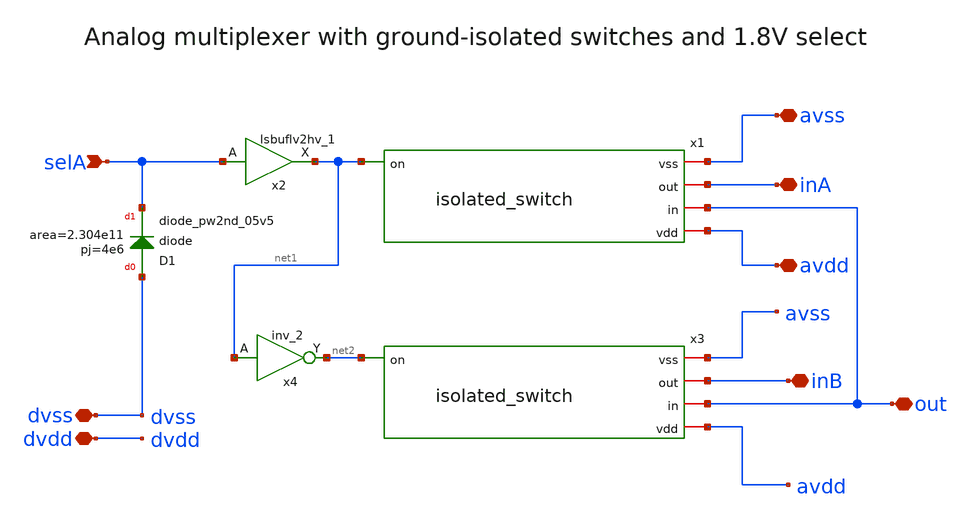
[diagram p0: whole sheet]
** sch_path: xschem/analog_mux_sel1v8.sch
**.subckt analog_mux_sel1v8 selA avss out inA avdd inB dvdd dvss
*.ipin selA
*.iopin avss
*.iopin out
*.iopin inA
*.iopin avdd
*.iopin inB
*.iopin dvdd
*.iopin dvss
x1 net1 avss inA out avdd isolated_switch
x2 selA dvdd dvss dvss avdd avdd net1 sky130_fd_sc_hvl__lsbuflv2hv_1
x3 net2 avss inB out avdd isolated_switch
x4 net1 dvss dvss avdd avdd net2 sky130_fd_sc_hvl__inv_2
XD1 dvss selA sky130_fd_pr__diode_pw2nd_05v5 area=2.304e11 pj=4e6
**.ends

* expanding   symbol:  isolated_switch.sym # of pins=5
** sym_path: xschem/isolated_switch.sym
** sch_path: xschem/isolated_switch.sch
.subckt isolated_switch on vss out in vdd
*.ipin on
*.iopin out
*.iopin vdd
*.iopin vss
*.iopin in
XM1 in onp net1 vss sky130_fd_pr__nfet_g5v0d10v5 L=0.5 W=8 nf=2 ad='int((nf+1)/2) * W/nf * 0.29' as='int((nf+2)/2) * W/nf * 0.29'
+ pd='2*int((nf+1)/2) * (W/nf + 0.29)' ps='2*int((nf+2)/2) * (W/nf + 0.29)' nrd='0.29 / W' nrs='0.29 / W'
+ sa=0 sb=0 sd=0 mult=1 m=1
XM2 in onb net1 vdd sky130_fd_pr__pfet_g5v0d10v5 L=0.5 W=4 nf=2 ad='int((nf+1)/2) * W/nf * 0.29' as='int((nf+2)/2) * W/nf * 0.29'
+ pd='2*int((nf+1)/2) * (W/nf + 0.29)' ps='2*int((nf+2)/2) * (W/nf + 0.29)' nrd='0.29 / W' nrs='0.29 / W'
+ sa=0 sb=0 sd=0 mult=1 m=1
XM3 net1 onb net1 vss sky130_fd_pr__nfet_g5v0d10v5 L=0.5 W=4 nf=1 ad='int((nf+1)/2) * W/nf * 0.29' as='int((nf+2)/2) * W/nf * 0.29'
+ pd='2*int((nf+1)/2) * (W/nf + 0.29)' ps='2*int((nf+2)/2) * (W/nf + 0.29)' nrd='0.29 / W' nrs='0.29 / W'
+ sa=0 sb=0 sd=0 mult=1 m=1
XM4 net1 onp net1 vdd sky130_fd_pr__pfet_g5v0d10v5 L=0.5 W=2 nf=1 ad='int((nf+1)/2) * W/nf * 0.29' as='int((nf+2)/2) * W/nf * 0.29'
+ pd='2*int((nf+1)/2) * (W/nf + 0.29)' ps='2*int((nf+2)/2) * (W/nf + 0.29)' nrd='0.29 / W' nrs='0.29 / W'
+ sa=0 sb=0 sd=0 mult=1 m=1
XM5 in onb in vss sky130_fd_pr__nfet_g5v0d10v5 L=0.5 W=4 nf=1 ad='int((nf+1)/2) * W/nf * 0.29' as='int((nf+2)/2) * W/nf * 0.29'
+ pd='2*int((nf+1)/2) * (W/nf + 0.29)' ps='2*int((nf+2)/2) * (W/nf + 0.29)' nrd='0.29 / W' nrs='0.29 / W'
+ sa=0 sb=0 sd=0 mult=1 m=1
XM6 in onp in vdd sky130_fd_pr__pfet_g5v0d10v5 L=0.5 W=2 nf=1 ad='int((nf+1)/2) * W/nf * 0.29' as='int((nf+2)/2) * W/nf * 0.29'
+ pd='2*int((nf+1)/2) * (W/nf + 0.29)' ps='2*int((nf+2)/2) * (W/nf + 0.29)' nrd='0.29 / W' nrs='0.29 / W'
+ sa=0 sb=0 sd=0 mult=1 m=1
XM7 onb on vdd vdd sky130_fd_pr__pfet_g5v0d10v5 L=0.5 W=2 nf=2 ad='int((nf+1)/2) * W/nf * 0.29' as='int((nf+2)/2) * W/nf * 0.29'
+ pd='2*int((nf+1)/2) * (W/nf + 0.29)' ps='2*int((nf+2)/2) * (W/nf + 0.29)' nrd='0.29 / W' nrs='0.29 / W'
+ sa=0 sb=0 sd=0 mult=1 m=1
XM8 onb on vss vss sky130_fd_pr__nfet_g5v0d10v5 L=0.5 W=2 nf=1 ad='int((nf+1)/2) * W/nf * 0.29' as='int((nf+2)/2) * W/nf * 0.29'
+ pd='2*int((nf+1)/2) * (W/nf + 0.29)' ps='2*int((nf+2)/2) * (W/nf + 0.29)' nrd='0.29 / W' nrs='0.29 / W'
+ sa=0 sb=0 sd=0 mult=1 m=1
XM9 onp onb vdd vdd sky130_fd_pr__pfet_g5v0d10v5 L=0.5 W=2 nf=2 ad='int((nf+1)/2) * W/nf * 0.29' as='int((nf+2)/2) * W/nf * 0.29'
+ pd='2*int((nf+1)/2) * (W/nf + 0.29)' ps='2*int((nf+2)/2) * (W/nf + 0.29)' nrd='0.29 / W' nrs='0.29 / W'
+ sa=0 sb=0 sd=0 mult=1 m=1
XM10 onp onb vss vss sky130_fd_pr__nfet_g5v0d10v5 L=0.5 W=2 nf=1 ad='int((nf+1)/2) * W/nf * 0.29' as='int((nf+2)/2) * W/nf * 0.29'
+ pd='2*int((nf+1)/2) * (W/nf + 0.29)' ps='2*int((nf+2)/2) * (W/nf + 0.29)' nrd='0.29 / W' nrs='0.29 / W'
+ sa=0 sb=0 sd=0 mult=1 m=1
XXD1 vss on sky130_fd_pr__diode_pw2nd_05v5 area=2.025e11 pj=4e6
XM11 net1 onp out vss sky130_fd_pr__nfet_g5v0d10v5 L=0.5 W=8 nf=2 ad='int((nf+1)/2) * W/nf * 0.29' as='int((nf+2)/2) * W/nf * 0.29'
+ pd='2*int((nf+1)/2) * (W/nf + 0.29)' ps='2*int((nf+2)/2) * (W/nf + 0.29)' nrd='0.29 / W' nrs='0.29 / W'
+ sa=0 sb=0 sd=0 mult=1 m=1
XM12 net1 onb out vdd sky130_fd_pr__pfet_g5v0d10v5 L=0.5 W=4 nf=2 ad='int((nf+1)/2) * W/nf * 0.29' as='int((nf+2)/2) * W/nf * 0.29'
+ pd='2*int((nf+1)/2) * (W/nf + 0.29)' ps='2*int((nf+2)/2) * (W/nf + 0.29)' nrd='0.29 / W' nrs='0.29 / W'
+ sa=0 sb=0 sd=0 mult=1 m=1
XM13 out onb out vss sky130_fd_pr__nfet_g5v0d10v5 L=0.5 W=4 nf=1 ad='int((nf+1)/2) * W/nf * 0.29' as='int((nf+2)/2) * W/nf * 0.29'
+ pd='2*int((nf+1)/2) * (W/nf + 0.29)' ps='2*int((nf+2)/2) * (W/nf + 0.29)' nrd='0.29 / W' nrs='0.29 / W'
+ sa=0 sb=0 sd=0 mult=1 m=1
XM14 out onp out vdd sky130_fd_pr__pfet_g5v0d10v5 L=0.5 W=2 nf=1 ad='int((nf+1)/2) * W/nf * 0.29' as='int((nf+2)/2) * W/nf * 0.29'
+ pd='2*int((nf+1)/2) * (W/nf + 0.29)' ps='2*int((nf+2)/2) * (W/nf + 0.29)' nrd='0.29 / W' nrs='0.29 / W'
+ sa=0 sb=0 sd=0 mult=1 m=1
XM15 net1 onb net1 vss sky130_fd_pr__nfet_g5v0d10v5 L=0.5 W=4 nf=1 ad='int((nf+1)/2) * W/nf * 0.29' as='int((nf+2)/2) * W/nf * 0.29'
+ pd='2*int((nf+1)/2) * (W/nf + 0.29)' ps='2*int((nf+2)/2) * (W/nf + 0.29)' nrd='0.29 / W' nrs='0.29 / W'
+ sa=0 sb=0 sd=0 mult=1 m=1
XM16 net1 onp net1 vdd sky130_fd_pr__pfet_g5v0d10v5 L=0.5 W=2 nf=1 ad='int((nf+1)/2) * W/nf * 0.29' as='int((nf+2)/2) * W/nf * 0.29'
+ pd='2*int((nf+1)/2) * (W/nf + 0.29)' ps='2*int((nf+2)/2) * (W/nf + 0.29)' nrd='0.29 / W' nrs='0.29 / W'
+ sa=0 sb=0 sd=0 mult=1 m=1
XM17 vss onb net1 vss sky130_fd_pr__nfet_g5v0d10v5 L=0.5 W=1 nf=1 ad='int((nf+1)/2) * W/nf * 0.29' as='int((nf+2)/2) * W/nf * 0.29'
+ pd='2*int((nf+1)/2) * (W/nf + 0.29)' ps='2*int((nf+2)/2) * (W/nf + 0.29)' nrd='0.29 / W' nrs='0.29 / W'
+ sa=0 sb=0 sd=0 mult=1 m=1
.ends

.end
